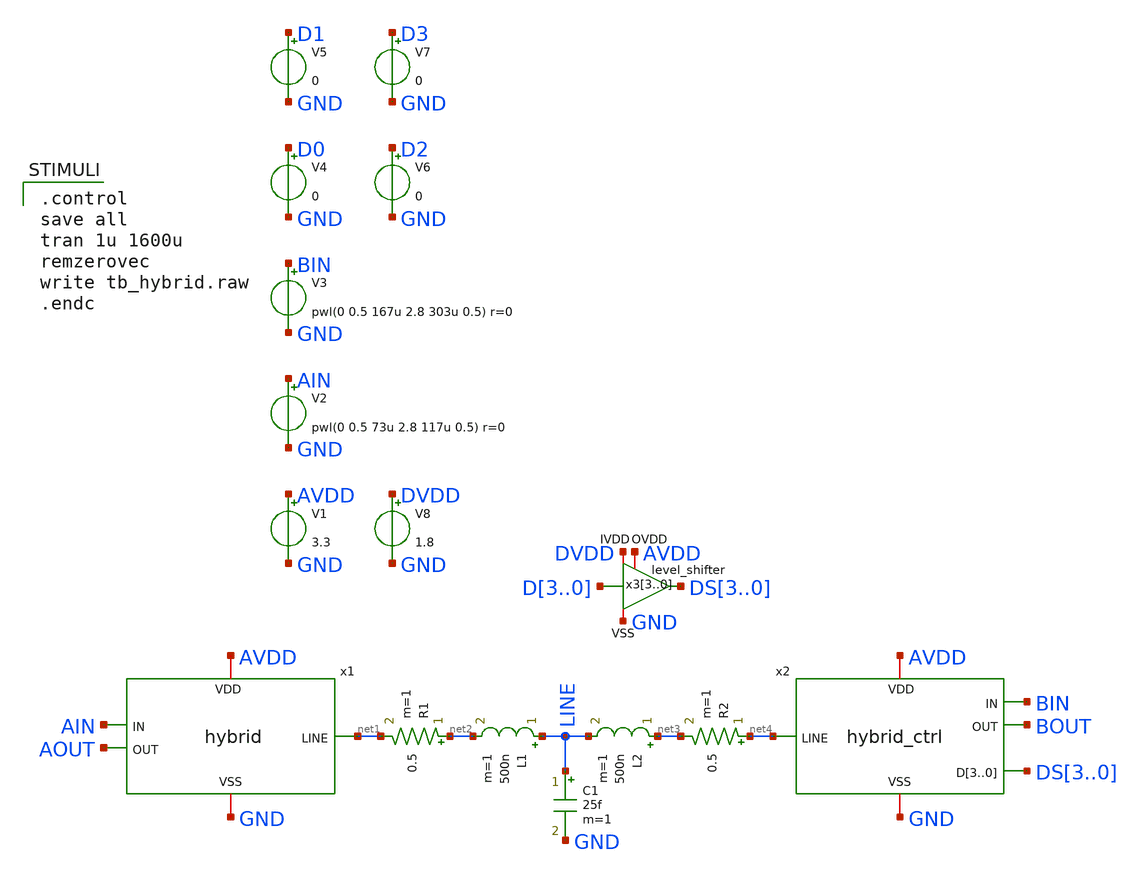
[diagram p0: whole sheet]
** sch_path: xschem/tb_hybrid.sch
**.subckt tb_hybrid
V1 AVDD GND 3.3
V2 AIN GND pwl(0 0.5 73u 2.8 117u 0.5) r=0
V3 BIN GND pwl(0 0.5 167u 2.8 303u 0.5) r=0
V4 D0 GND 0
V5 D1 GND 0
V6 D2 GND 0
V7 D3 GND 0
x1 AVDD AIN net1 AOUT GND hybrid
x2 AVDD BIN net4 DS3 DS2 DS1 DS0 BOUT GND hybrid_ctrl
L1 LINE net2 500n m=1
R1 net2 net1 0.5 m=1
R2 net4 net3 0.5 m=1
L2 net3 LINE 500n m=1
C1 LINE GND 25f m=1
x33 AVDD DVDD DS3 D3 GND level_shifter
x32 AVDD DVDD DS2 D2 GND level_shifter
x31 AVDD DVDD DS1 D1 GND level_shifter
x30 AVDD DVDD DS0 D0 GND level_shifter
V8 DVDD GND 1.8
**** begin user architecture code

.control
save all
tran 1u 1600u
remzerovec
write tb_hybrid.raw
.endc


 .lib $::SKYWATER_MODELS/sky130.lib.spice tt
.include $::SKYWATER_STDCELLS/sky130_fd_sc_hd.spice

**** end user architecture code
**.ends
.end
